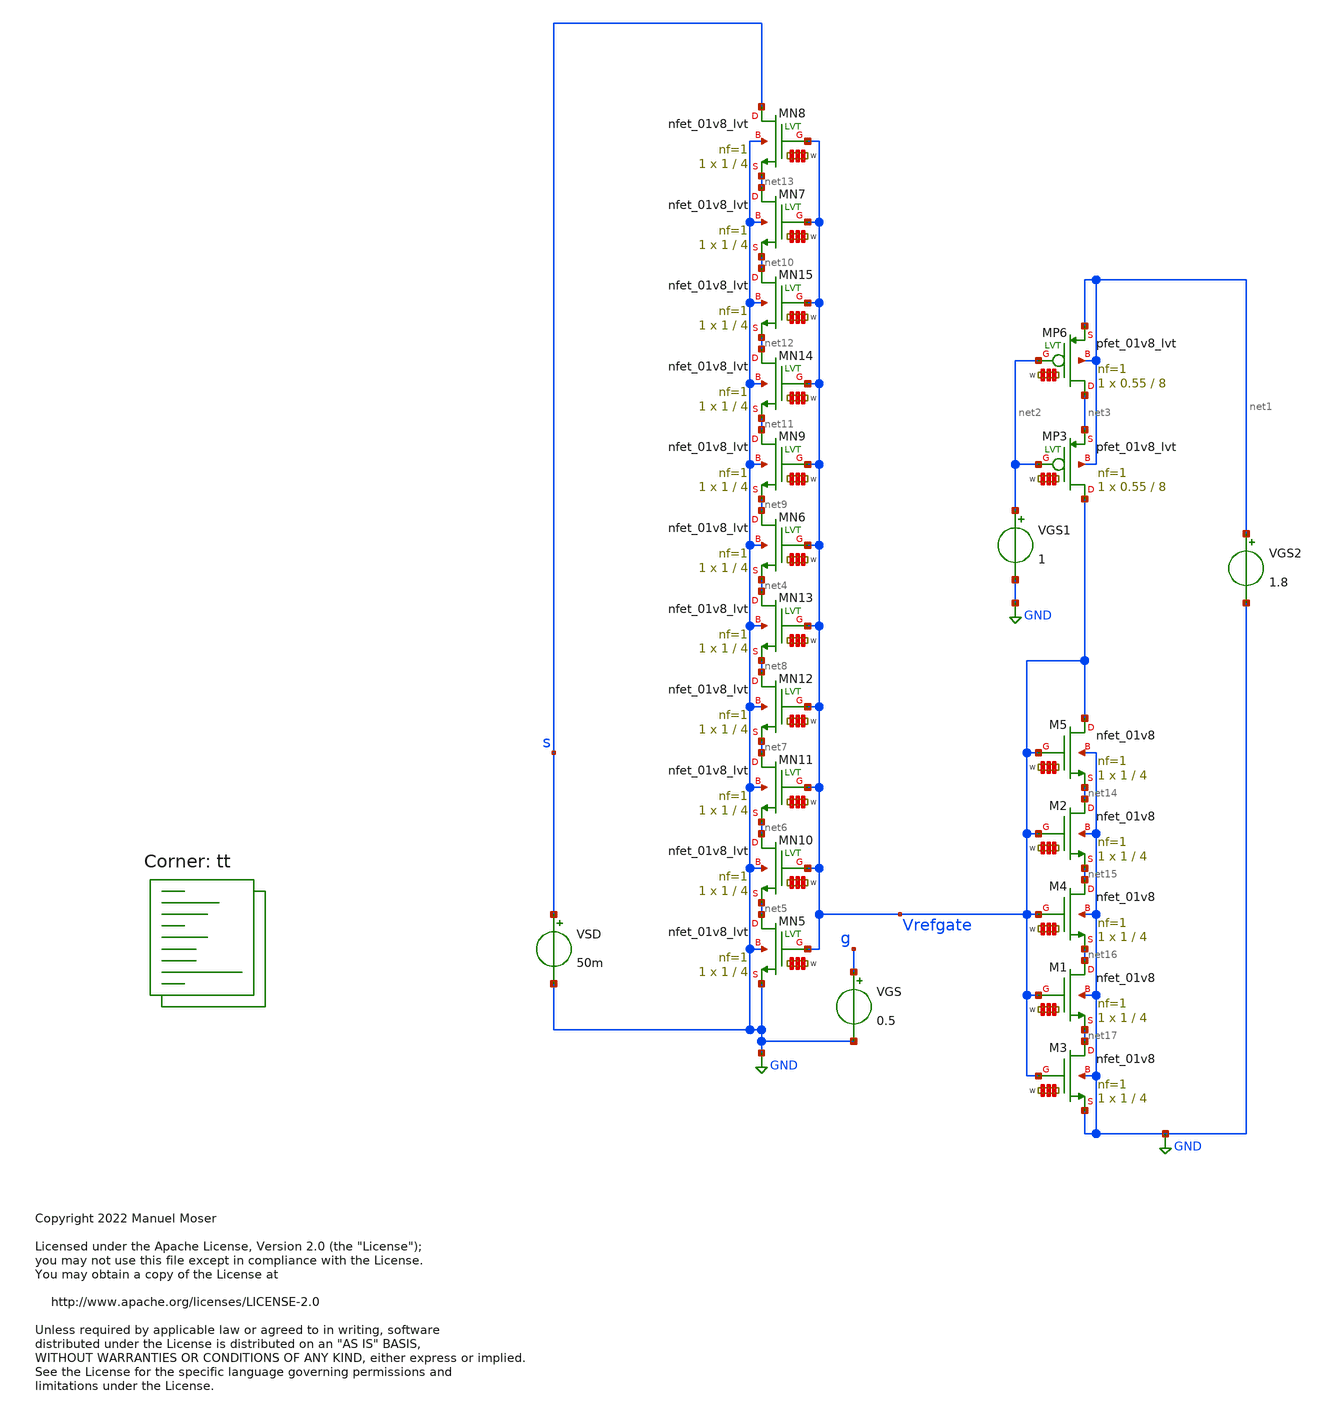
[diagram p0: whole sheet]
** sch_path: xschem/archive/isource_res_transistor_tb.sch
* Copyright 2022 Manuel Moser
* Licensed under the Apache License, Version 2.0 (the "License");
**.subckt isource_res_transistor_tb
VSD s GND 50m
VGS g GND 0.5
XMP3 Vrefgate net2 net3 net1 sky130_fd_pr__pfet_01v8_lvt L=8 W='0.55 * 1 ' nf=1 ad='int((nf+1)/2) * W / nf * 0.29'
+ as='int((nf+2)/2) * W / nf * 0.29' pd='2*int((nf+1)/2) * (W / nf + 0.29)' ps='2*int((nf+2)/2) * (W / nf + 0.29)'
+ nrd='0.29 / W ' nrs='0.29 / W ' sa=0 sb=0 sd=0 mult=1 m=1
XMP6 net3 net2 net1 net1 sky130_fd_pr__pfet_01v8_lvt L=8 W='0.55 * 1 ' nf=1 ad='int((nf+1)/2) * W / nf * 0.29'
+ as='int((nf+2)/2) * W / nf * 0.29' pd='2*int((nf+1)/2) * (W / nf + 0.29)' ps='2*int((nf+2)/2) * (W / nf + 0.29)'
+ nrd='0.29 / W ' nrs='0.29 / W ' sa=0 sb=0 sd=0 mult=1 m=1
VGS1 net2 GND 1
VGS2 net1 GND 1.8
XMN5 net5 Vrefgate GND GND sky130_fd_pr__nfet_01v8_lvt L=4 W='1 * 1 ' nf=1 ad='int((nf+1)/2) * W / nf * 0.29'
+ as='int((nf+2)/2) * W / nf * 0.29' pd='2*int((nf+1)/2) * (W / nf + 0.29)' ps='2*int((nf+2)/2) * (W / nf + 0.29)'
+ nrd='0.29 / W ' nrs='0.29 / W ' sa=0 sb=0 sd=0 mult=1 m=1
XMN6 net9 Vrefgate net4 GND sky130_fd_pr__nfet_01v8_lvt L=4 W='1 * 1 ' nf=1 ad='int((nf+1)/2) * W / nf * 0.29'
+ as='int((nf+2)/2) * W / nf * 0.29' pd='2*int((nf+1)/2) * (W / nf + 0.29)' ps='2*int((nf+2)/2) * (W / nf + 0.29)'
+ nrd='0.29 / W ' nrs='0.29 / W ' sa=0 sb=0 sd=0 mult=1 m=1
XMN9 net11 Vrefgate net9 GND sky130_fd_pr__nfet_01v8_lvt L=4 W='1 * 1 ' nf=1 ad='int((nf+1)/2) * W / nf * 0.29'
+ as='int((nf+2)/2) * W / nf * 0.29' pd='2*int((nf+1)/2) * (W / nf + 0.29)' ps='2*int((nf+2)/2) * (W / nf + 0.29)'
+ nrd='0.29 / W ' nrs='0.29 / W ' sa=0 sb=0 sd=0 mult=1 m=1
XMN10 net6 Vrefgate net5 GND sky130_fd_pr__nfet_01v8_lvt L=4 W='1 * 1 ' nf=1 ad='int((nf+1)/2) * W / nf * 0.29'
+ as='int((nf+2)/2) * W / nf * 0.29' pd='2*int((nf+1)/2) * (W / nf + 0.29)' ps='2*int((nf+2)/2) * (W / nf + 0.29)'
+ nrd='0.29 / W ' nrs='0.29 / W ' sa=0 sb=0 sd=0 mult=1 m=1
XMN11 net7 Vrefgate net6 GND sky130_fd_pr__nfet_01v8_lvt L=4 W='1 * 1 ' nf=1 ad='int((nf+1)/2) * W / nf * 0.29'
+ as='int((nf+2)/2) * W / nf * 0.29' pd='2*int((nf+1)/2) * (W / nf + 0.29)' ps='2*int((nf+2)/2) * (W / nf + 0.29)'
+ nrd='0.29 / W ' nrs='0.29 / W ' sa=0 sb=0 sd=0 mult=1 m=1
XMN12 net8 Vrefgate net7 GND sky130_fd_pr__nfet_01v8_lvt L=4 W='1 * 1 ' nf=1 ad='int((nf+1)/2) * W / nf * 0.29'
+ as='int((nf+2)/2) * W / nf * 0.29' pd='2*int((nf+1)/2) * (W / nf + 0.29)' ps='2*int((nf+2)/2) * (W / nf + 0.29)'
+ nrd='0.29 / W ' nrs='0.29 / W ' sa=0 sb=0 sd=0 mult=1 m=1
XMN13 net4 Vrefgate net8 GND sky130_fd_pr__nfet_01v8_lvt L=4 W='1 * 1 ' nf=1 ad='int((nf+1)/2) * W / nf * 0.29'
+ as='int((nf+2)/2) * W / nf * 0.29' pd='2*int((nf+1)/2) * (W / nf + 0.29)' ps='2*int((nf+2)/2) * (W / nf + 0.29)'
+ nrd='0.29 / W ' nrs='0.29 / W ' sa=0 sb=0 sd=0 mult=1 m=1
XMN7 net13 Vrefgate net10 GND sky130_fd_pr__nfet_01v8_lvt L=4 W='1 * 1 ' nf=1 ad='int((nf+1)/2) * W / nf * 0.29'
+ as='int((nf+2)/2) * W / nf * 0.29' pd='2*int((nf+1)/2) * (W / nf + 0.29)' ps='2*int((nf+2)/2) * (W / nf + 0.29)'
+ nrd='0.29 / W ' nrs='0.29 / W ' sa=0 sb=0 sd=0 mult=1 m=1
XMN8 s Vrefgate net13 GND sky130_fd_pr__nfet_01v8_lvt L=4 W='1 * 1 ' nf=1 ad='int((nf+1)/2) * W / nf * 0.29'
+ as='int((nf+2)/2) * W / nf * 0.29' pd='2*int((nf+1)/2) * (W / nf + 0.29)' ps='2*int((nf+2)/2) * (W / nf + 0.29)'
+ nrd='0.29 / W ' nrs='0.29 / W ' sa=0 sb=0 sd=0 mult=1 m=1
XMN14 net12 Vrefgate net11 GND sky130_fd_pr__nfet_01v8_lvt L=4 W='1 * 1 ' nf=1 ad='int((nf+1)/2) * W / nf * 0.29'
+ as='int((nf+2)/2) * W / nf * 0.29' pd='2*int((nf+1)/2) * (W / nf + 0.29)' ps='2*int((nf+2)/2) * (W / nf + 0.29)'
+ nrd='0.29 / W ' nrs='0.29 / W ' sa=0 sb=0 sd=0 mult=1 m=1
XMN15 net10 Vrefgate net12 GND sky130_fd_pr__nfet_01v8_lvt L=4 W='1 * 1 ' nf=1 ad='int((nf+1)/2) * W / nf * 0.29'
+ as='int((nf+2)/2) * W / nf * 0.29' pd='2*int((nf+1)/2) * (W / nf + 0.29)' ps='2*int((nf+2)/2) * (W / nf + 0.29)'
+ nrd='0.29 / W ' nrs='0.29 / W ' sa=0 sb=0 sd=0 mult=1 m=1
XM2 net14 Vrefgate net15 GND sky130_fd_pr__nfet_01v8 L=4 W='1 * 1 ' nf=1 ad='int((nf+1)/2) * W / nf * 0.29'
+ as='int((nf+2)/2) * W / nf * 0.29' pd='2*int((nf+1)/2) * (W / nf + 0.29)' ps='2*int((nf+2)/2) * (W / nf + 0.29)'
+ nrd='0.29 / W ' nrs='0.29 / W ' sa=0 sb=0 sd=0 mult=1 m=1
XM3 net17 Vrefgate GND GND sky130_fd_pr__nfet_01v8 L=4 W='1 * 1 ' nf=1 ad='int((nf+1)/2) * W / nf * 0.29'
+ as='int((nf+2)/2) * W / nf * 0.29' pd='2*int((nf+1)/2) * (W / nf + 0.29)' ps='2*int((nf+2)/2) * (W / nf + 0.29)'
+ nrd='0.29 / W ' nrs='0.29 / W ' sa=0 sb=0 sd=0 mult=1 m=1
XM1 net16 Vrefgate net17 GND sky130_fd_pr__nfet_01v8 L=4 W='1 * 1 ' nf=1 ad='int((nf+1)/2) * W / nf * 0.29'
+ as='int((nf+2)/2) * W / nf * 0.29' pd='2*int((nf+1)/2) * (W / nf + 0.29)' ps='2*int((nf+2)/2) * (W / nf + 0.29)'
+ nrd='0.29 / W ' nrs='0.29 / W ' sa=0 sb=0 sd=0 mult=1 m=1
XM4 net15 Vrefgate net16 GND sky130_fd_pr__nfet_01v8 L=4 W='1 * 1 ' nf=1 ad='int((nf+1)/2) * W / nf * 0.29'
+ as='int((nf+2)/2) * W / nf * 0.29' pd='2*int((nf+1)/2) * (W / nf + 0.29)' ps='2*int((nf+2)/2) * (W / nf + 0.29)'
+ nrd='0.29 / W ' nrs='0.29 / W ' sa=0 sb=0 sd=0 mult=1 m=1
XM5 Vrefgate Vrefgate net14 GND sky130_fd_pr__nfet_01v8 L=4 W='1 * 1 ' nf=1 ad='int((nf+1)/2) * W / nf * 0.29'
+ as='int((nf+2)/2) * W / nf * 0.29' pd='2*int((nf+1)/2) * (W / nf + 0.29)' ps='2*int((nf+2)/2) * (W / nf + 0.29)'
+ nrd='0.29 / W ' nrs='0.29 / W ' sa=0 sb=0 sd=0 mult=1 m=1
**** begin user architecture code



.temp 27

.save all
.save @m.xm1.msky130_fd_pr__pfet_01v8_lvt[Vth]
.save @m.xm1.msky130_fd_pr__pfet_01v8_lvt[gm]

.control
set num_threads=12
dc VSD 0 200m 1m
plot (vrefgate)
plot (70m/(-i(vsd)))
plot (-i(vsd))
plot @m.xm1.msky130_fd_pr__pfet_01v8_lvt[gm]

op
write pmos_power_transistor_tb.raw
print v(@m.xm1.msky130_fd_pr__pfet_01v8_lvt[Vth])

.endc



.lib $::SKYWATER_MODELS/sky130.lib.spice tt
**** end user architecture code
**.ends
.GLOBAL GND
.end
